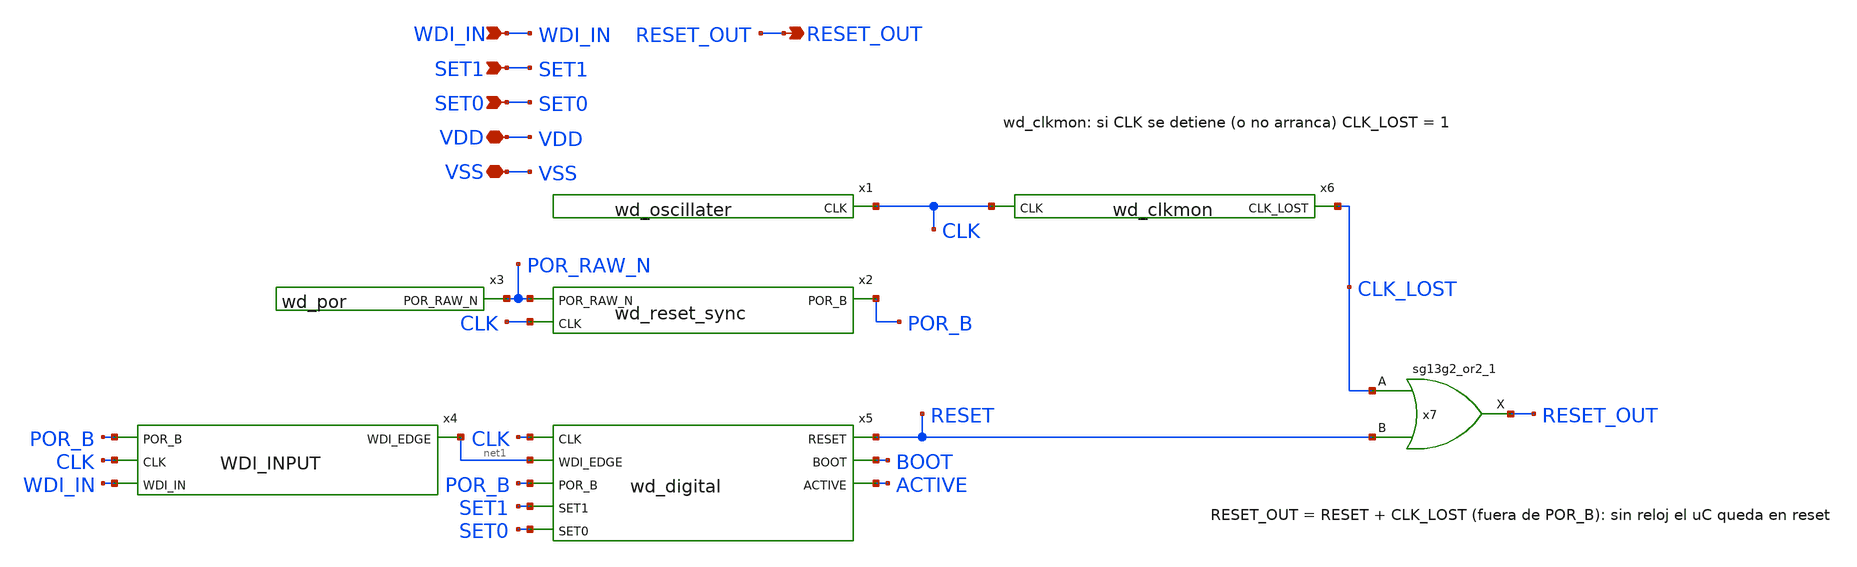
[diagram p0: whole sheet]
** sch_path: design/top/schematic/wd_watchdog.sch
**.subckt wd_watchdog SET1 SET0 WDI_IN RESET_OUT VDD VSS
*.ipin SET1
*.ipin SET0
*.ipin WDI_IN
*.opin RESET_OUT
*.iopin VDD
*.iopin VSS
x1 CLK VDD VSS wd_oscillater
x2 POR_RAW_N CLK POR_B VDD VSS wd_reset_sync
x3 POR_RAW_N VDD VSS wd_por
x4 POR_B CLK WDI_IN net1 WDI_INPUT
x5 RESET BOOT CLK net1 ACTIVE POR_B SET1 SET0 VDD VSS wd_digital
x6 CLK CLK_LOST VDD VSS wd_clkmon
x7 RESET_OUT CLK_LOST RESET VDD VSS sg13g2_or2_1
**.ends
.end
